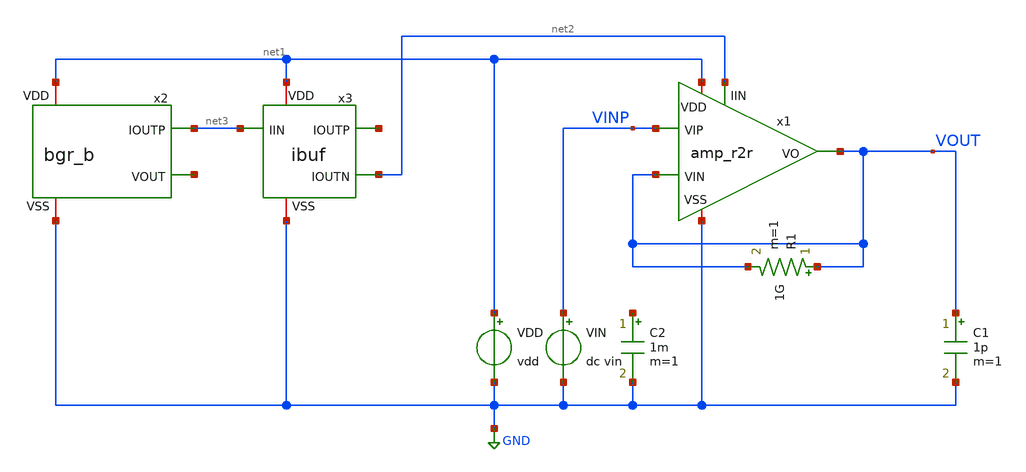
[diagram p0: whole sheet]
** sch_path: member_project/imager/YuMaehashi/design/tb_amp_r2r.sch
**.subckt tb_amp_r2r
x1 net1 VINP VOUT VOUT net2 GND amp_r2r
VDD net1 GND vdd
VIN VINP GND dc vin
C1 VOUT GND 1p m=1
x2 net1 net3 net4 GND bgr_b
x3 net1 net5 net3 net2 GND ibuf
R1 VOUT VOUT 1G m=1
C2 net6 GND 1m m=1
**** begin user architecture code


.option savecurrents
.temp 40
.param vdd = 5
.param vin = vdd/2
.control
set units=degree
save all

alterparam vthMN = 0 ; Slow:0.1, Fast:-0.1
alterparam vthMP = 0 ; Slow:-0.1, Fast:0.1
alterparam magRS = 1 ; Slow:1.2, Fast:0.85
reset

op

set mosprefix = m.x1.xx
set mossuffix = .m1

let i = 1
while i le 8
	set mp = {$mosprefix}mp{$&i}{$mossuffix}
	let id_val = @{$mp}[id]
	let vds_val = @{$mp}[vds]
	let vgs_val = @{$mp}[vgs]
	echo 'Mp{$&i}: Id=$&id_val Vds=$&vds_val Vgs=$&vgs_val'
	let i = i + 1
end
let i = 1
while i le 8
	set mn = {$mosprefix}mn{$&i}{$mossuffix}
	let id_val = @{$mn}[id]
	let vds_val = @{$mn}[vds]
	let vgs_val = @{$mn}[vgs]
	echo 'Mn{$&i}: Id=$&id_val Vds=$&vds_val Vgs=$&vgs_val'
	let i = i + 1
end


dc VIN 0 5 0.1
plot v(VINP) v(VOUT)
plot v(VOUT) - v(VINP)


.endc

 .include $::LIB/ip62_models
**** end user architecture code
**.ends
.GLOBAL GND
.end
